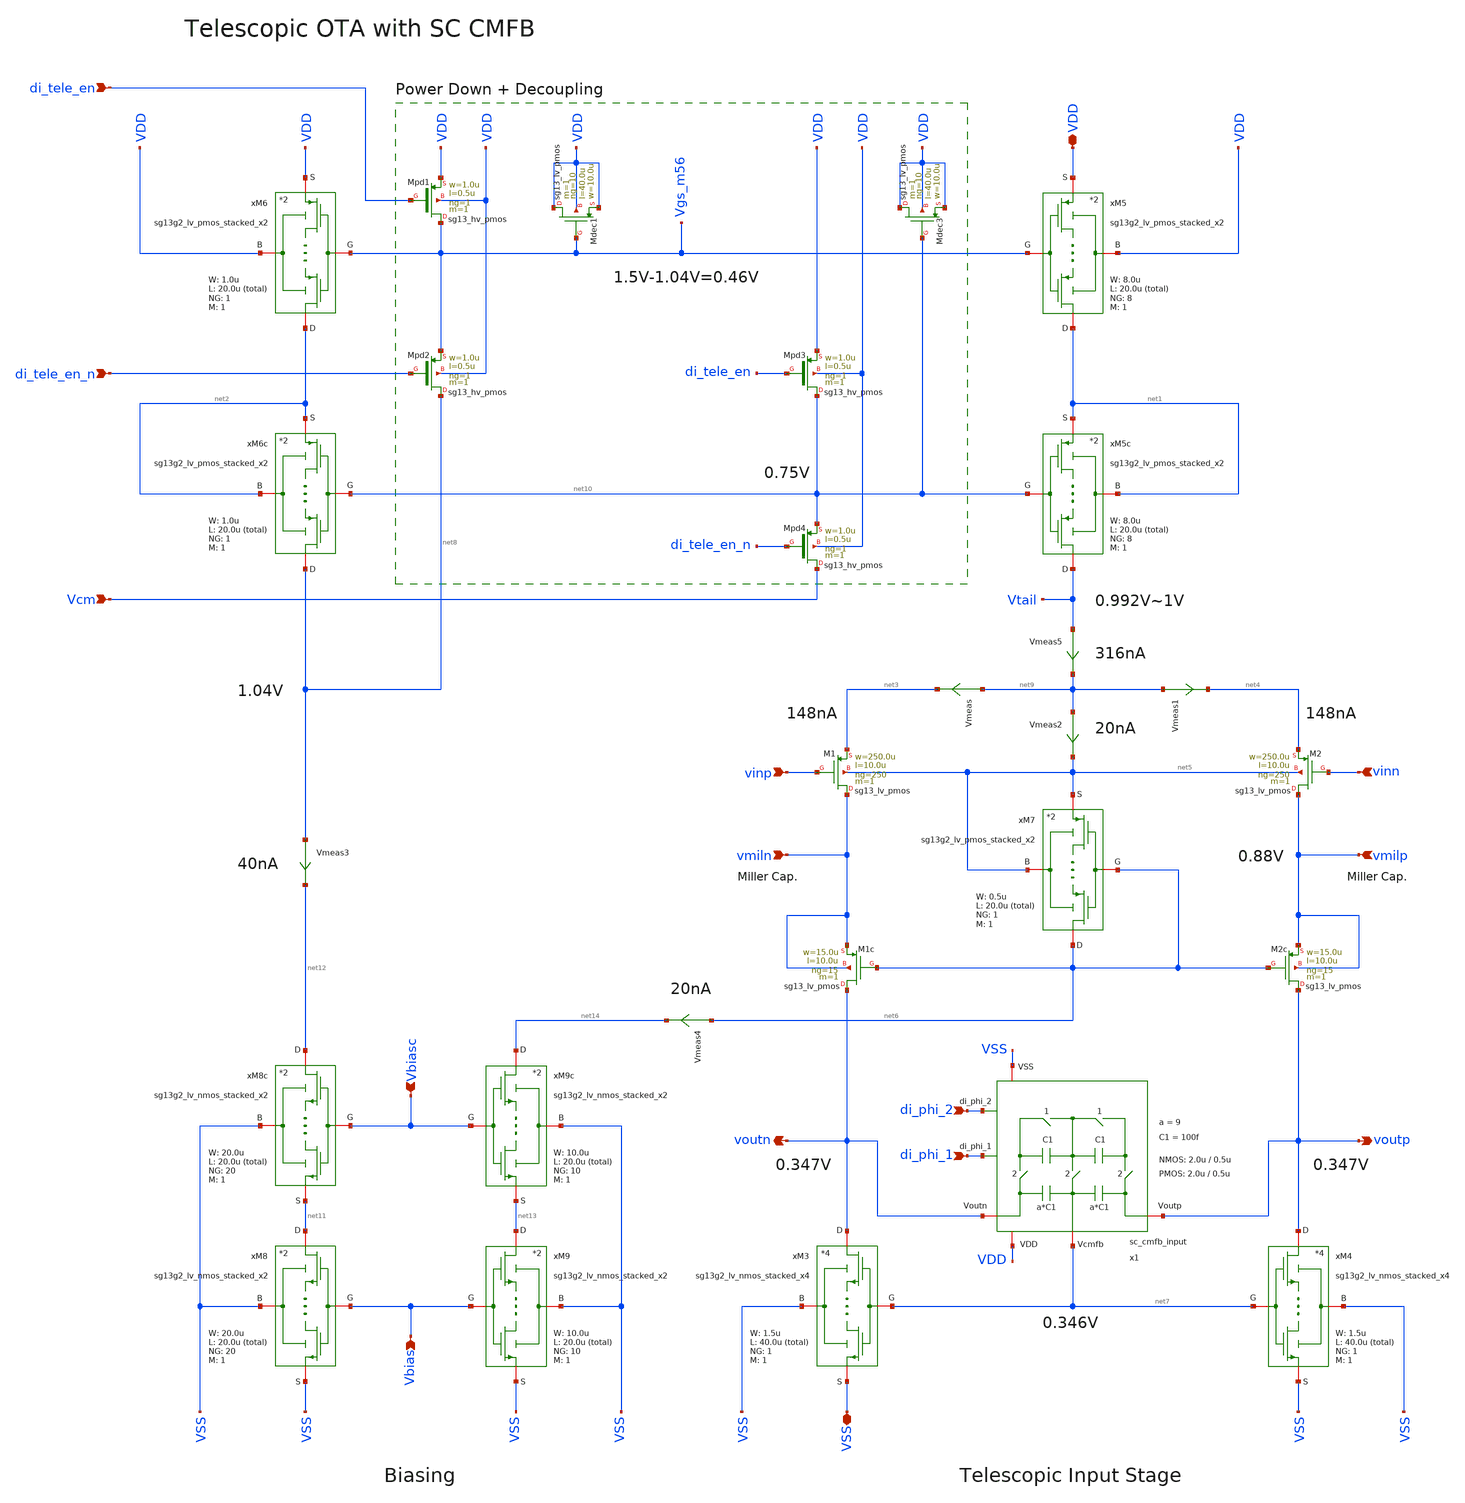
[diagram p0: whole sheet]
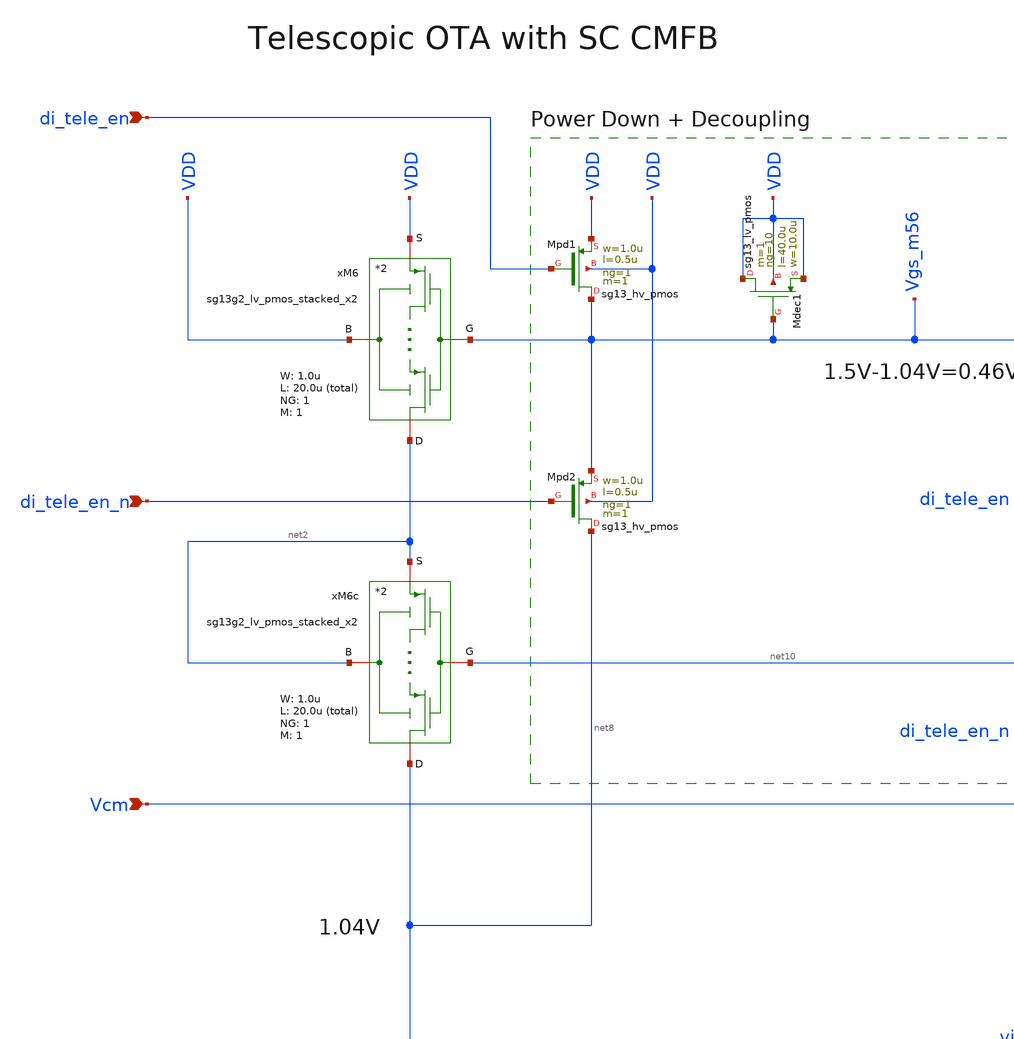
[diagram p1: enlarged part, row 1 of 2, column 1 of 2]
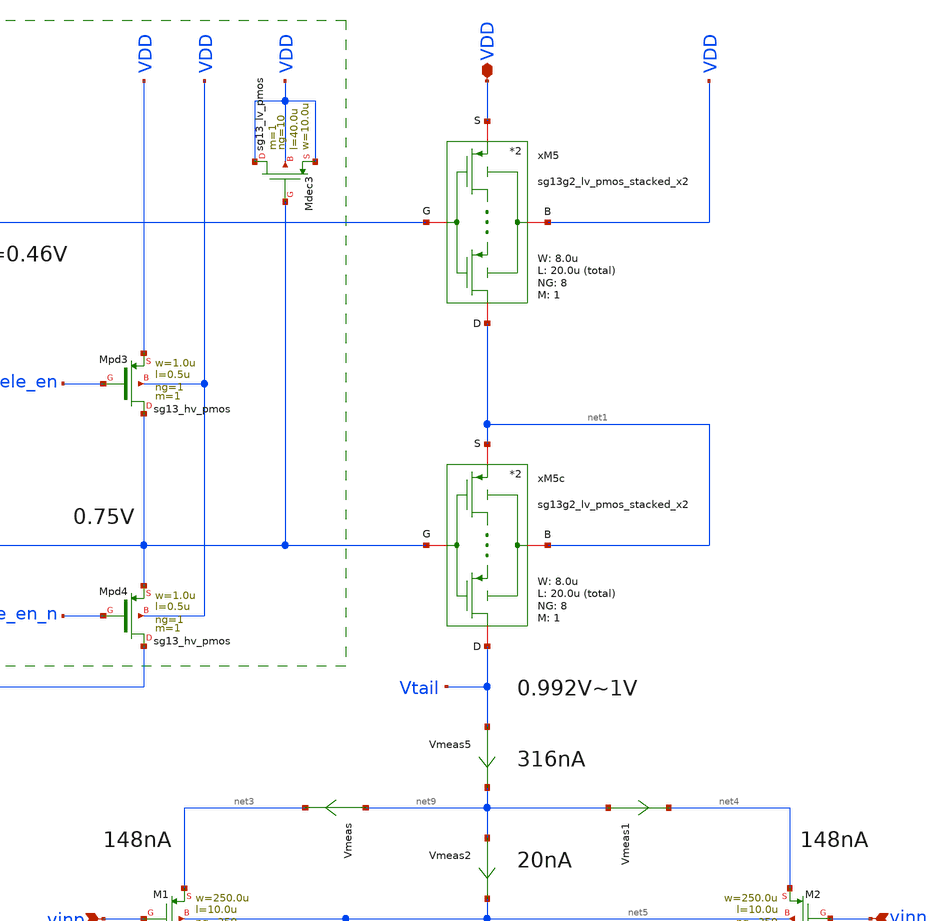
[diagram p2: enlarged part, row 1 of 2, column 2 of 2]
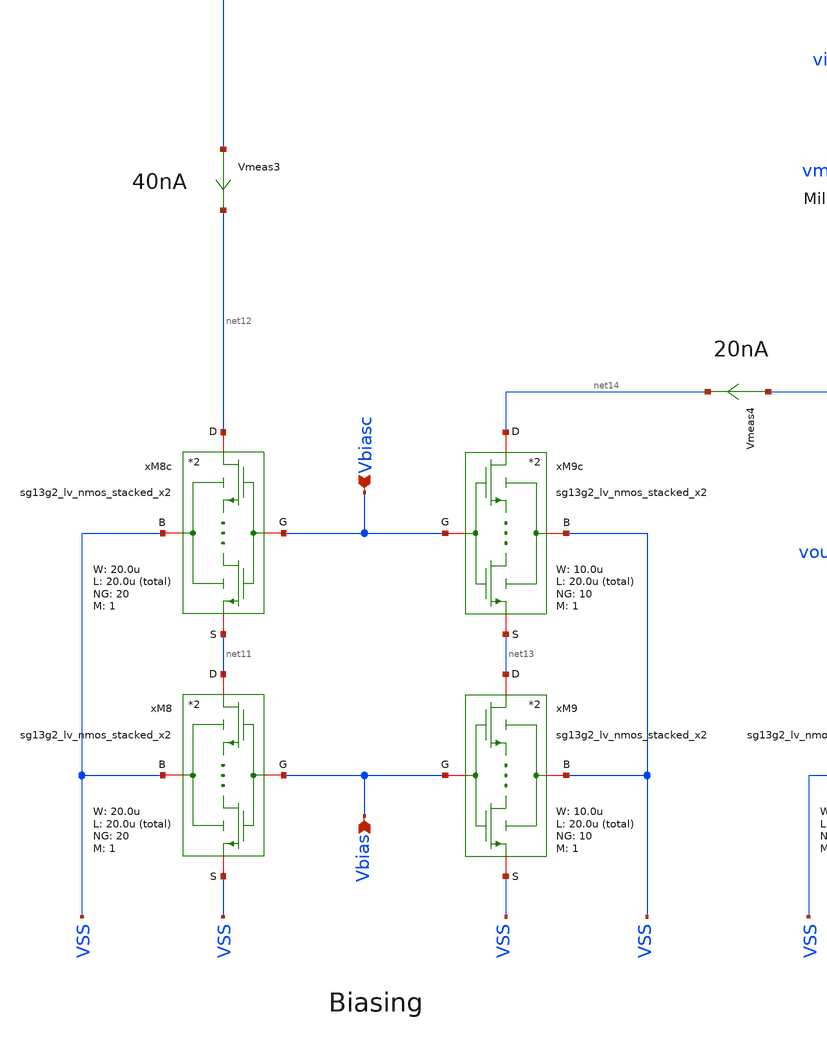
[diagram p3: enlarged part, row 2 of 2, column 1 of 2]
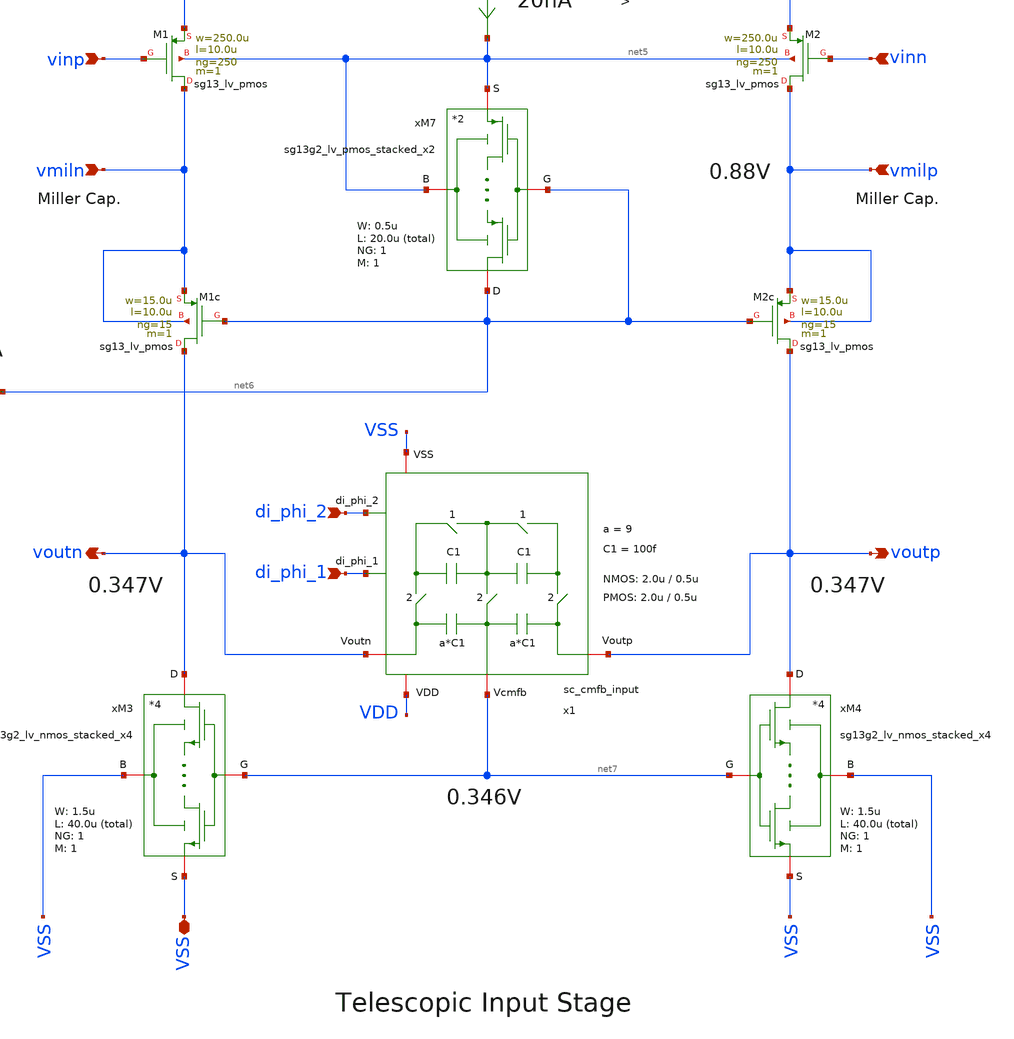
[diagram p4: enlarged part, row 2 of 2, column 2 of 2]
** sch_path: SG13G2_ATBS-ADC-main/xschem/bio_amplifier/amplifier_core/telescopic_ota/telescopic_ota.sch
**.subckt telescopic_ota di_phi_1 di_phi_2 vinp vinn voutp voutn VDD VSS Vcm di_tele_en di_tele_en_n
*+ vmilp vmiln Vbias Vbiasc
*.ipin di_phi_1
*.ipin di_phi_2
*.ipin vinp
*.ipin vinn
*.opin voutp
*.opin voutn
*.iopin VDD
*.iopin VSS
*.ipin Vcm
*.ipin di_tele_en
*.ipin di_tele_en_n
*.ipin vmilp
*.ipin vmiln
*.ipin Vbias
*.ipin Vbiasc
x1 di_phi_1 di_phi_2 VDD voutp VSS net7 voutn sc_cmfb_input W_P_CMFB=2.0u L_P_CMFB=0.5u
+ W_N_CMFB=2.0u L_N_CMFB=0.5u C1=100f a=9
xM6 net2 Vgs_m56 VDD VDD sg13g2_lv_pmos_stacked_x2 W_P=1.0u L_P=20.0u NG_P=1 M_P=1
xM5 net1 Vgs_m56 VDD VDD sg13g2_lv_pmos_stacked_x2 W_P=8.0u L_P=20.0u NG_P=8 M_P=1
xM5c Vtail net10 net1 net1 sg13g2_lv_pmos_stacked_x2 W_P=8.0u L_P=20.0u NG_P=8 M_P=1
xM7 net6 net6 net5 net5 sg13g2_lv_pmos_stacked_x2 W_P=0.5u L_P=20.0u NG_P=1 M_P=1
XM1 vmiln vinp net3 net5 sg13_lv_pmos w=250.0u l=10.0u ng=250 m=1 mm_ok=1
XM1c voutn net6 vmiln vmiln sg13_lv_pmos w=15.0u l=10.0u ng=15 m=1 mm_ok=1
XM2c voutp net6 vmilp vmilp sg13_lv_pmos w=15.0u l=10.0u ng=15 m=1 mm_ok=1
XM2 vmilp vinn net4 net5 sg13_lv_pmos w=250.0u l=10.0u ng=250 m=1 mm_ok=1
xM3 voutn net7 VSS VSS sg13g2_lv_nmos_stacked_x4 W_N=1.5u L_N=40.0u NG_N=1 M_N=1
xM4 voutp net7 VSS VSS sg13g2_lv_nmos_stacked_x4 W_N=1.5u L_N=40.0u NG_N=1 M_N=1
Vmeas net9 net3 0
.save i(vmeas)
Vmeas1 net9 net4 0
.save i(vmeas1)
Vmeas2 net9 net5 0
.save i(vmeas2)
xM6c net8 net10 net2 net2 sg13g2_lv_pmos_stacked_x2 W_P=1.0u L_P=20.0u NG_P=1 M_P=1
XMpd4 Vcm di_tele_en_n net10 VDD sg13_hv_pmos w=1.0u l=0.5u ng=1 m=1 mm_ok=1
XMdec1 VDD Vgs_m56 VDD VDD sg13_lv_pmos w=10.0u l=40.0u ng=10 m=1 mm_ok=1
XMpd3 net10 di_tele_en VDD VDD sg13_hv_pmos w=1.0u l=0.5u ng=1 m=1 mm_ok=1
XMpd2 net8 di_tele_en_n Vgs_m56 VDD sg13_hv_pmos w=1.0u l=0.5u ng=1 m=1 mm_ok=1
XMpd1 Vgs_m56 di_tele_en VDD VDD sg13_hv_pmos w=1.0u l=0.5u ng=1 m=1 mm_ok=1
XMdec3 VDD net10 VDD VDD sg13_lv_pmos w=10.0u l=40.0u ng=10 m=1 mm_ok=1
Vmeas3 net8 net12 0
.save i(vmeas3)
Vmeas4 net6 net14 0
.save i(vmeas4)
xM8c net12 Vbiasc VSS net11 sg13g2_lv_nmos_stacked_x2 W_N=20.0u L_N=20.0u NG_N=20 M_N=1
xM8 net11 Vbias VSS VSS sg13g2_lv_nmos_stacked_x2 W_N=20.0u L_N=20.0u NG_N=20 M_N=1
xM9c net14 Vbiasc VSS net13 sg13g2_lv_nmos_stacked_x2 W_N=10.0u L_N=20.0u NG_N=10 M_N=1
xM9 net13 Vbias VSS VSS sg13g2_lv_nmos_stacked_x2 W_N=10.0u L_N=20.0u NG_N=10 M_N=1
Vmeas5 Vtail net9 0
.save i(vmeas5)
**.ends

* expanding   symbol:  bio_amplifier/amplifier_core/sc_cmfb/sc_cmfb_input.sym # of pins=7
** sym_path: SG13G2_ATBS-ADC-main/xschem/bio_amplifier/amplifier_core/sc_cmfb/sc_cmfb_input.sym
** sch_path: SG13G2_ATBS-ADC-main/xschem/bio_amplifier/amplifier_core/sc_cmfb/sc_cmfb_input.sch
.subckt sc_cmfb_input di_phi_1 di_phi_2 VDD Voutp VSS Vcmfb Voutn  W_P_CMFB=2.0u L_P_CMFB=0.5u
+ W_N_CMFB=2.0u L_N_CMFB=0.5u C1=100f a=9
*.iopin VSS
*.iopin VDD
*.iopin Vcmfb
*.iopin Voutp
*.iopin Voutn
*.ipin di_phi_1
*.ipin di_phi_2
x1 VDD di_phi_2 VSS net1 Voutp di_phi_2_n transmission_gate_lv_wo_dummy W_P=W_P_CMFB L_P=L_P_CMFB
+ W_N=W_N_CMFB L_N=L_N_CMFB
C1 Voutp Vcmfb {a*C1} m=1
x2 VDD di_phi_2 VSS net2 Vcmfb di_phi_2_n transmission_gate_lv_wo_dummy W_P=W_P_CMFB L_P=L_P_CMFB
+ W_N=W_N_CMFB L_N=L_N_CMFB
x3 VDD di_phi_2 VSS net3 Voutn di_phi_2_n transmission_gate_lv_wo_dummy W_P=W_P_CMFB L_P=L_P_CMFB
+ W_N=W_N_CMFB L_N=L_N_CMFB
x4 VDD di_phi_1 VSS net2 net1 di_phi_1_n transmission_gate_lv_wo_dummy W_P=W_P_CMFB L_P=L_P_CMFB
+ W_N=W_N_CMFB L_N=L_N_CMFB
x5 VDD di_phi_1 VSS net2 net3 di_phi_1_n transmission_gate_lv_wo_dummy W_P=W_P_CMFB L_P=L_P_CMFB
+ W_N=W_N_CMFB L_N=L_N_CMFB
C2 Vcmfb Voutn {a*C1} m=1
C3 net1 net2 C1 m=1
C4 net2 net3 C1 m=1
x7 VDD di_phi_1 di_phi_1_n VSS inverter_lv W_P=W_P_CMFB L_P=L_P_CMFB W_N=W_N_CMFB L_N=L_N_CMFB
x6 VDD di_phi_2 di_phi_2_n VSS inverter_lv W_P=W_P_CMFB L_P=L_P_CMFB W_N=W_N_CMFB L_N=L_N_CMFB
.ends


* expanding   symbol:  stacked_transistors/sg13g2_lv_pmos_stacked/sg13g2_lv_pmos_stacked_x2.sym # of
*+ pins=4
** sym_path: SG13G2_ATBS-ADC-main/xschem/stacked_transistors/sg13g2_lv_pmos_stacked/sg13g2_lv_pmos_stacked_x2.sym
** sch_path: SG13G2_ATBS-ADC-main/xschem/stacked_transistors/sg13g2_lv_pmos_stacked/sg13g2_lv_pmos_stacked_x2.sch
.subckt sg13g2_lv_pmos_stacked_x2 D G B S  W_P=1.0u L_P=0.45u NG_P=1 M_P=1
*.iopin D
*.iopin S
*.iopin G
*.iopin B
XM1 net1 G S B sg13_lv_pmos w=W_P l=L_P/2 ng=NG_P m=M_P mm_ok=1
XM2 D G net1 B sg13_lv_pmos w=W_P l=L_P/2 ng=NG_P m=M_P mm_ok=1
.ends


* expanding   symbol:  stacked_transistors/sg13g2_lv_nmos_stacked/sg13g2_lv_nmos_stacked_x4.sym # of
*+ pins=4
** sym_path: SG13G2_ATBS-ADC-main/xschem/stacked_transistors/sg13g2_lv_nmos_stacked/sg13g2_lv_nmos_stacked_x4.sym
** sch_path: SG13G2_ATBS-ADC-main/xschem/stacked_transistors/sg13g2_lv_nmos_stacked/sg13g2_lv_nmos_stacked_x4.sch
.subckt sg13g2_lv_nmos_stacked_x4 D G B S  W_N=1.0u L_N=0.45u NG_N=1 M_N=1
*.iopin D
*.iopin S
*.iopin G
*.iopin B
XM1 net1 G S B sg13_lv_nmos w=W_N l=L_N/4 ng=NG_N m=M_N mm_ok=1
XM2 net3 G net1 B sg13_lv_nmos w=W_N l=L_N/4 ng=NG_N m=M_N mm_ok=1
XM3 net2 G net3 B sg13_lv_nmos w=W_N l=L_N/4 ng=NG_N m=M_N mm_ok=1
XM4 D G net2 B sg13_lv_nmos w=W_N l=L_N/4 ng=NG_N m=M_N mm_ok=1
.ends


* expanding   symbol:  stacked_transistors/sg13g2_lv_nmos_stacked/sg13g2_lv_nmos_stacked_x2.sym # of
*+ pins=4
** sym_path: SG13G2_ATBS-ADC-main/xschem/stacked_transistors/sg13g2_lv_nmos_stacked/sg13g2_lv_nmos_stacked_x2.sym
** sch_path: SG13G2_ATBS-ADC-main/xschem/stacked_transistors/sg13g2_lv_nmos_stacked/sg13g2_lv_nmos_stacked_x2.sch
.subckt sg13g2_lv_nmos_stacked_x2 D G B S  W_N=1.0u L_N=0.45u NG_N=1 M_N=1
*.iopin D
*.iopin S
*.iopin G
*.iopin B
XM1 net1 G S B sg13_lv_nmos w=W_N l=L_N/2 ng=NG_N m=M_N mm_ok=1
XM2 D G net1 B sg13_lv_nmos w=W_N l=L_N/2 ng=NG_N m=M_N mm_ok=1
.ends


* expanding   symbol:  transmission_gate/transmission_gate_lv_wo_dummy.sym # of pins=6
** sym_path: SG13G2_ATBS-ADC-main/xschem/transmission_gate/transmission_gate_lv_wo_dummy.sym
** sch_path: SG13G2_ATBS-ADC-main/xschem/transmission_gate/transmission_gate_lv_wo_dummy.sch
.subckt transmission_gate_lv_wo_dummy VDD di_tg_ctrl VSS v_b v_a di_tg_ctrl_n  W_P=1.0u L_P=0.13u
+ W_N=1.0u L_N=0.13u
*.iopin v_a
*.iopin v_b
*.iopin VDD
*.iopin VSS
*.ipin di_tg_ctrl
*.ipin di_tg_ctrl_n
XM1 v_a di_tg_ctrl v_b VSS sg13_lv_nmos w=W_N l=L_N ng=1 m=1 mm_ok=1
XM2 v_a di_tg_ctrl_n v_b VDD sg13_lv_pmos w=W_P l=L_P ng=1 m=1 mm_ok=1
.ends


* expanding   symbol:  inverter/inverter_lv.sym # of pins=4
** sym_path: SG13G2_ATBS-ADC-main/xschem/inverter/inverter_lv.sym
** sch_path: SG13G2_ATBS-ADC-main/xschem/inverter/inverter_lv.sch
.subckt inverter_lv VDD vin vout VSS  W_P=3.0u L_P=0.13u W_N=1.0u L_N=0.13u
*.ipin vin
*.iopin VDD
*.iopin VSS
*.opin vout
XM1 vout vin VDD VDD sg13_lv_pmos w=W_P l=L_P ng=1 m=1 mm_ok=1
XM2 vout vin VSS VSS sg13_lv_nmos w=W_N l=L_N ng=1 m=1 mm_ok=1
.ends

.end
